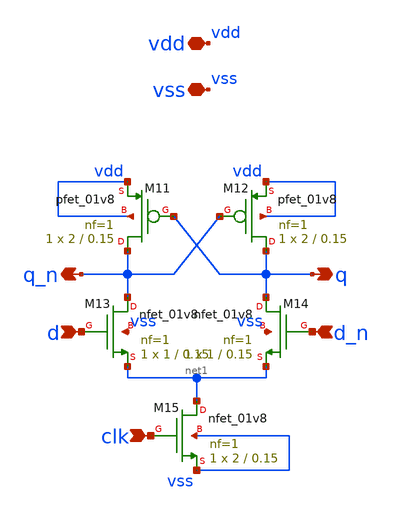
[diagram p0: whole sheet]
** sch_path: xschem/latch.sch
**.subckt latch vdd d q vss d_n q_n clk
*.iopin vdd
*.ipin d
*.opin q
*.iopin vss
*.ipin d_n
*.opin q_n
*.ipin clk
XM11 q_n q vdd vdd sky130_fd_pr__pfet_01v8 L=0.15 W=2 nf=1 ad='int((nf+1)/2) * W/nf * 0.29' as='int((nf+2)/2) * W/nf * 0.29'
+ pd='2*int((nf+1)/2) * (W/nf + 0.29)' ps='2*int((nf+2)/2) * (W/nf + 0.29)' nrd='0.29 / W' nrs='0.29 / W'
+ sa=0 sb=0 sd=0 mult=1 m=1
XM12 q q_n vdd vdd sky130_fd_pr__pfet_01v8 L=0.15 W=2 nf=1 ad='int((nf+1)/2) * W/nf * 0.29' as='int((nf+2)/2) * W/nf * 0.29'
+ pd='2*int((nf+1)/2) * (W/nf + 0.29)' ps='2*int((nf+2)/2) * (W/nf + 0.29)' nrd='0.29 / W' nrs='0.29 / W'
+ sa=0 sb=0 sd=0 mult=1 m=1
XM13 q_n d net1 vss sky130_fd_pr__nfet_01v8 L=0.15 W=1 nf=1 ad='int((nf+1)/2) * W/nf * 0.29' as='int((nf+2)/2) * W/nf * 0.29'
+ pd='2*int((nf+1)/2) * (W/nf + 0.29)' ps='2*int((nf+2)/2) * (W/nf + 0.29)' nrd='0.29 / W' nrs='0.29 / W'
+ sa=0 sb=0 sd=0 mult=1 m=1
XM14 q d_n net1 vss sky130_fd_pr__nfet_01v8 L=0.15 W=1 nf=1 ad='int((nf+1)/2) * W/nf * 0.29' as='int((nf+2)/2) * W/nf * 0.29'
+ pd='2*int((nf+1)/2) * (W/nf + 0.29)' ps='2*int((nf+2)/2) * (W/nf + 0.29)' nrd='0.29 / W' nrs='0.29 / W'
+ sa=0 sb=0 sd=0 mult=1 m=1
XM15 net1 clk vss vss sky130_fd_pr__nfet_01v8 L=0.15 W=2 nf=1 ad='int((nf+1)/2) * W/nf * 0.29' as='int((nf+2)/2) * W/nf * 0.29'
+ pd='2*int((nf+1)/2) * (W/nf + 0.29)' ps='2*int((nf+2)/2) * (W/nf + 0.29)' nrd='0.29 / W' nrs='0.29 / W'
+ sa=0 sb=0 sd=0 mult=1 m=1
**.ends
.end
